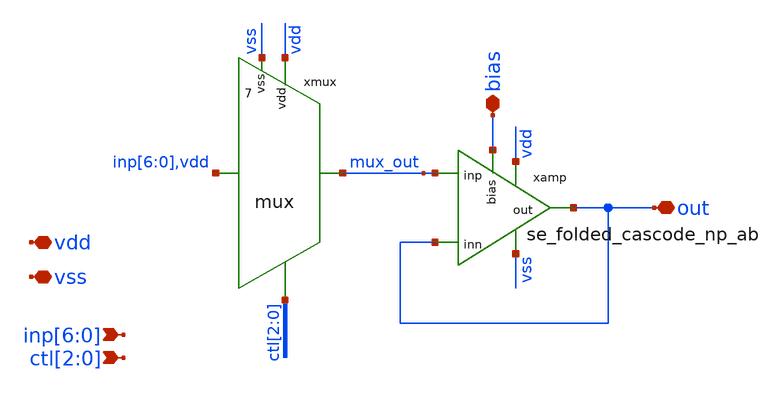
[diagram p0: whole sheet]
** sch_path: xschem/testbuffer/testbuffer.sch
**.subckt testbuffer out vss vdd bias inp[6],inp[5],inp[4],inp[3],inp[2],inp[1],inp[0]
*+ ctl[2],ctl[1],ctl[0]
*.iopin out
*.iopin vss
*.iopin vdd
*.iopin bias
*.ipin inp[6],inp[5],inp[4],inp[3],inp[2],inp[1],inp[0]
*.ipin ctl[2],ctl[1],ctl[0]
xmux mux_out vdd vss inp[6] inp[5] inp[4] inp[3] inp[2] inp[1] inp[0] vdd ctl[2] ctl[1] ctl[0] mux
xamp vdd out mux_out out vss bias se_folded_cascode_np_ab
**.ends
.end
